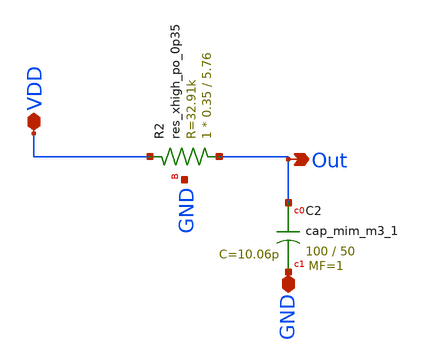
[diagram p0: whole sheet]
** sch_path: Schematic/RClay.sch
**.subckt RClay VDD Out GND
*.iopin VDD
*.opin Out
*.iopin GND
XR2 Out VDD GND sky130_fd_pr__res_xhigh_po_0p35 L=5.76 mult=1 m=1
XC2 Out GND sky130_fd_pr__cap_mim_m3_1 W=100 L=50 MF=1 m=1
**.ends
.end
